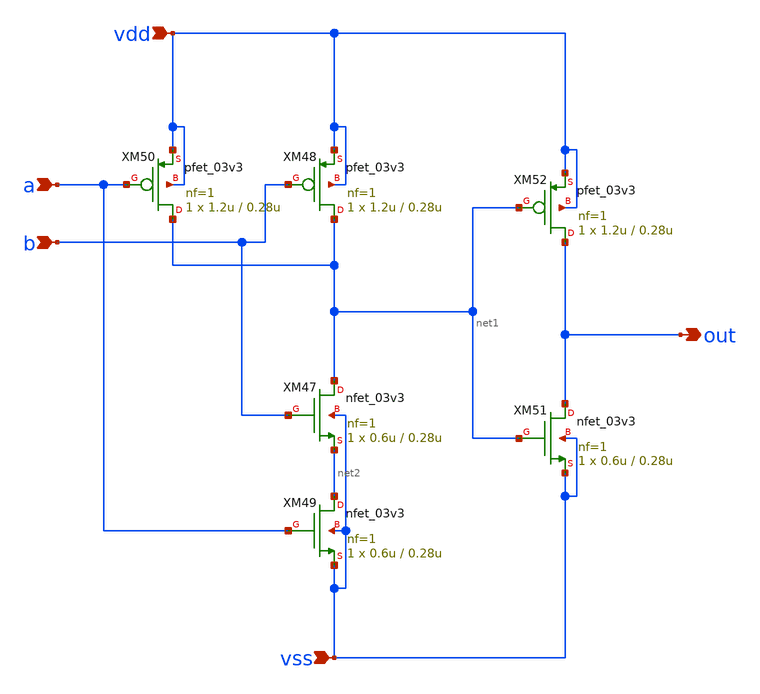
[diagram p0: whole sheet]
** sch_path: xschem/and2.sch
**.subckt and2 a b vdd vss out
*.ipin a
*.ipin b
*.ipin vdd
*.ipin vss
*.opin out
XM47 net1 b net2 vss nfet_03v3 L=0.28u W=0.6u nf=1 ad='int((nf+1)/2) * W/nf * 0.18u' as='int((nf+2)/2) * W/nf * 0.18u'
+ pd='2*int((nf+1)/2) * (W/nf + 0.18u)' ps='2*int((nf+2)/2) * (W/nf + 0.18u)' nrd='0.18u / W' nrs='0.18u / W'
+ sa=0 sb=0 sd=0 m=1
XM48 net1 b vdd vdd pfet_03v3 L=0.28u W=1.2u nf=1 ad='int((nf+1)/2) * W/nf * 0.18u' as='int((nf+2)/2) * W/nf * 0.18u'
+ pd='2*int((nf+1)/2) * (W/nf + 0.18u)' ps='2*int((nf+2)/2) * (W/nf + 0.18u)' nrd='0.18u / W' nrs='0.18u / W'
+ sa=0 sb=0 sd=0 m=1
XM49 net2 a vss vss nfet_03v3 L=0.28u W=0.6u nf=1 ad='int((nf+1)/2) * W/nf * 0.18u' as='int((nf+2)/2) * W/nf * 0.18u'
+ pd='2*int((nf+1)/2) * (W/nf + 0.18u)' ps='2*int((nf+2)/2) * (W/nf + 0.18u)' nrd='0.18u / W' nrs='0.18u / W'
+ sa=0 sb=0 sd=0 m=1
XM50 net1 a vdd vdd pfet_03v3 L=0.28u W=1.2u nf=1 ad='int((nf+1)/2) * W/nf * 0.18u' as='int((nf+2)/2) * W/nf * 0.18u'
+ pd='2*int((nf+1)/2) * (W/nf + 0.18u)' ps='2*int((nf+2)/2) * (W/nf + 0.18u)' nrd='0.18u / W' nrs='0.18u / W'
+ sa=0 sb=0 sd=0 m=1
XM51 out net1 vss vss nfet_03v3 L=0.28u W=0.6u nf=1 ad='int((nf+1)/2) * W/nf * 0.18u' as='int((nf+2)/2) * W/nf * 0.18u'
+ pd='2*int((nf+1)/2) * (W/nf + 0.18u)' ps='2*int((nf+2)/2) * (W/nf + 0.18u)' nrd='0.18u / W' nrs='0.18u / W'
+ sa=0 sb=0 sd=0 m=1
XM52 out net1 vdd vdd pfet_03v3 L=0.28u W=1.2u nf=1 ad='int((nf+1)/2) * W/nf * 0.18u' as='int((nf+2)/2) * W/nf * 0.18u'
+ pd='2*int((nf+1)/2) * (W/nf + 0.18u)' ps='2*int((nf+2)/2) * (W/nf + 0.18u)' nrd='0.18u / W' nrs='0.18u / W'
+ sa=0 sb=0 sd=0 m=1
**.ends
.end
